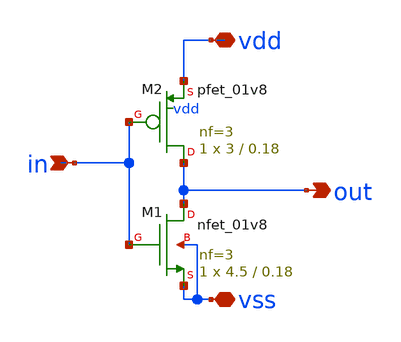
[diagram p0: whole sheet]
** sch_path: Day1/inverter/xschem/inverter.sch
**.subckt inverter in out vss vdd
*.ipin in
*.opin out
*.iopin vss
*.iopin vdd
XM1 out in vss vss sky130_fd_pr__nfet_01v8 L=0.18 W=4.5 nf=3 ad='int((nf+1)/2) * W/nf * 0.29' as='int((nf+2)/2) * W/nf * 0.29'
+ pd='2*int((nf+1)/2) * (W/nf + 0.29)' ps='2*int((nf+2)/2) * (W/nf + 0.29)' nrd='0.29 / W' nrs='0.29 / W'
+ sa=0 sb=0 sd=0 mult=1 m=1
XM2 out in vdd vdd sky130_fd_pr__pfet_01v8 L=0.18 W=3 nf=3 ad='int((nf+1)/2) * W/nf * 0.29' as='int((nf+2)/2) * W/nf * 0.29'
+ pd='2*int((nf+1)/2) * (W/nf + 0.29)' ps='2*int((nf+2)/2) * (W/nf + 0.29)' nrd='0.29 / W' nrs='0.29 / W'
+ sa=0 sb=0 sd=0 mult=1 m=1
**.ends
.end
